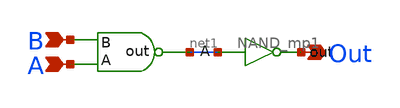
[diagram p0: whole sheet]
** sch_path: MP1/AND_MP1.sch
**.subckt AND_MP1 B A Out
*.ipin B
*.ipin A
*.opin Out
x1 B A net1 NAND_mp1
x2 Out net1 INV_mp1
**.ends

* expanding   symbol:  /home/madvlsi/Documents/MP1/NAND_mp1.sym # of pins=3
** sym_path: MP1/NAND_mp1.sym
** sch_path: MP1/NAND_mp1.sch
.subckt NAND_mp1 B A out
*.ipin A
*.ipin B
*.opin out
XM1 out A VDD VDD sky130_fd_pr__pfet_01v8 L=0.15 W=1 nf=1 ad='int((nf+1)/2) * W/nf * 0.29' as='int((nf+2)/2) * W/nf * 0.29'
+ pd='2*int((nf+1)/2) * (W/nf + 0.29)' ps='2*int((nf+2)/2) * (W/nf + 0.29)' nrd='0.29 / W' nrs='0.29 / W'
+ sa=0 sb=0 sd=0 mult=1 m=1
XM2 out B VDD VDD sky130_fd_pr__pfet_01v8 L=0.15 W=1 nf=1 ad='int((nf+1)/2) * W/nf * 0.29' as='int((nf+2)/2) * W/nf * 0.29'
+ pd='2*int((nf+1)/2) * (W/nf + 0.29)' ps='2*int((nf+2)/2) * (W/nf + 0.29)' nrd='0.29 / W' nrs='0.29 / W'
+ sa=0 sb=0 sd=0 mult=1 m=1
XM3 out A net1 GND sky130_fd_pr__nfet_01v8 L=0.15 W=1 nf=1 ad='int((nf+1)/2) * W/nf * 0.29' as='int((nf+2)/2) * W/nf * 0.29'
+ pd='2*int((nf+1)/2) * (W/nf + 0.29)' ps='2*int((nf+2)/2) * (W/nf + 0.29)' nrd='0.29 / W' nrs='0.29 / W'
+ sa=0 sb=0 sd=0 mult=1 m=1
XM5 net1 B GND GND sky130_fd_pr__nfet_01v8 L=0.15 W=1 nf=1 ad='int((nf+1)/2) * W/nf * 0.29' as='int((nf+2)/2) * W/nf * 0.29'
+ pd='2*int((nf+1)/2) * (W/nf + 0.29)' ps='2*int((nf+2)/2) * (W/nf + 0.29)' nrd='0.29 / W' nrs='0.29 / W'
+ sa=0 sb=0 sd=0 mult=1 m=1
.ends


* expanding   symbol:  /home/madvlsi/Documents/MP1/INV_mp1.sym # of pins=2
** sym_path: MP1/INV_mp1.sym
** sch_path: MP1/INV_mp1.sch
.subckt INV_mp1 out A
*.ipin A
*.opin out
XM1 out A VDD VDD sky130_fd_pr__pfet_01v8 L=0.15 W=1 nf=1 ad='int((nf+1)/2) * W/nf * 0.29' as='int((nf+2)/2) * W/nf * 0.29'
+ pd='2*int((nf+1)/2) * (W/nf + 0.29)' ps='2*int((nf+2)/2) * (W/nf + 0.29)' nrd='0.29 / W' nrs='0.29 / W'
+ sa=0 sb=0 sd=0 mult=1 m=1
XM2 out A GND GND sky130_fd_pr__nfet_01v8 L=0.15 W=1 nf=1 ad='int((nf+1)/2) * W/nf * 0.29' as='int((nf+2)/2) * W/nf * 0.29'
+ pd='2*int((nf+1)/2) * (W/nf + 0.29)' ps='2*int((nf+2)/2) * (W/nf + 0.29)' nrd='0.29 / W' nrs='0.29 / W'
+ sa=0 sb=0 sd=0 mult=1 m=1
.ends

.GLOBAL VDD
.GLOBAL GND
.end
